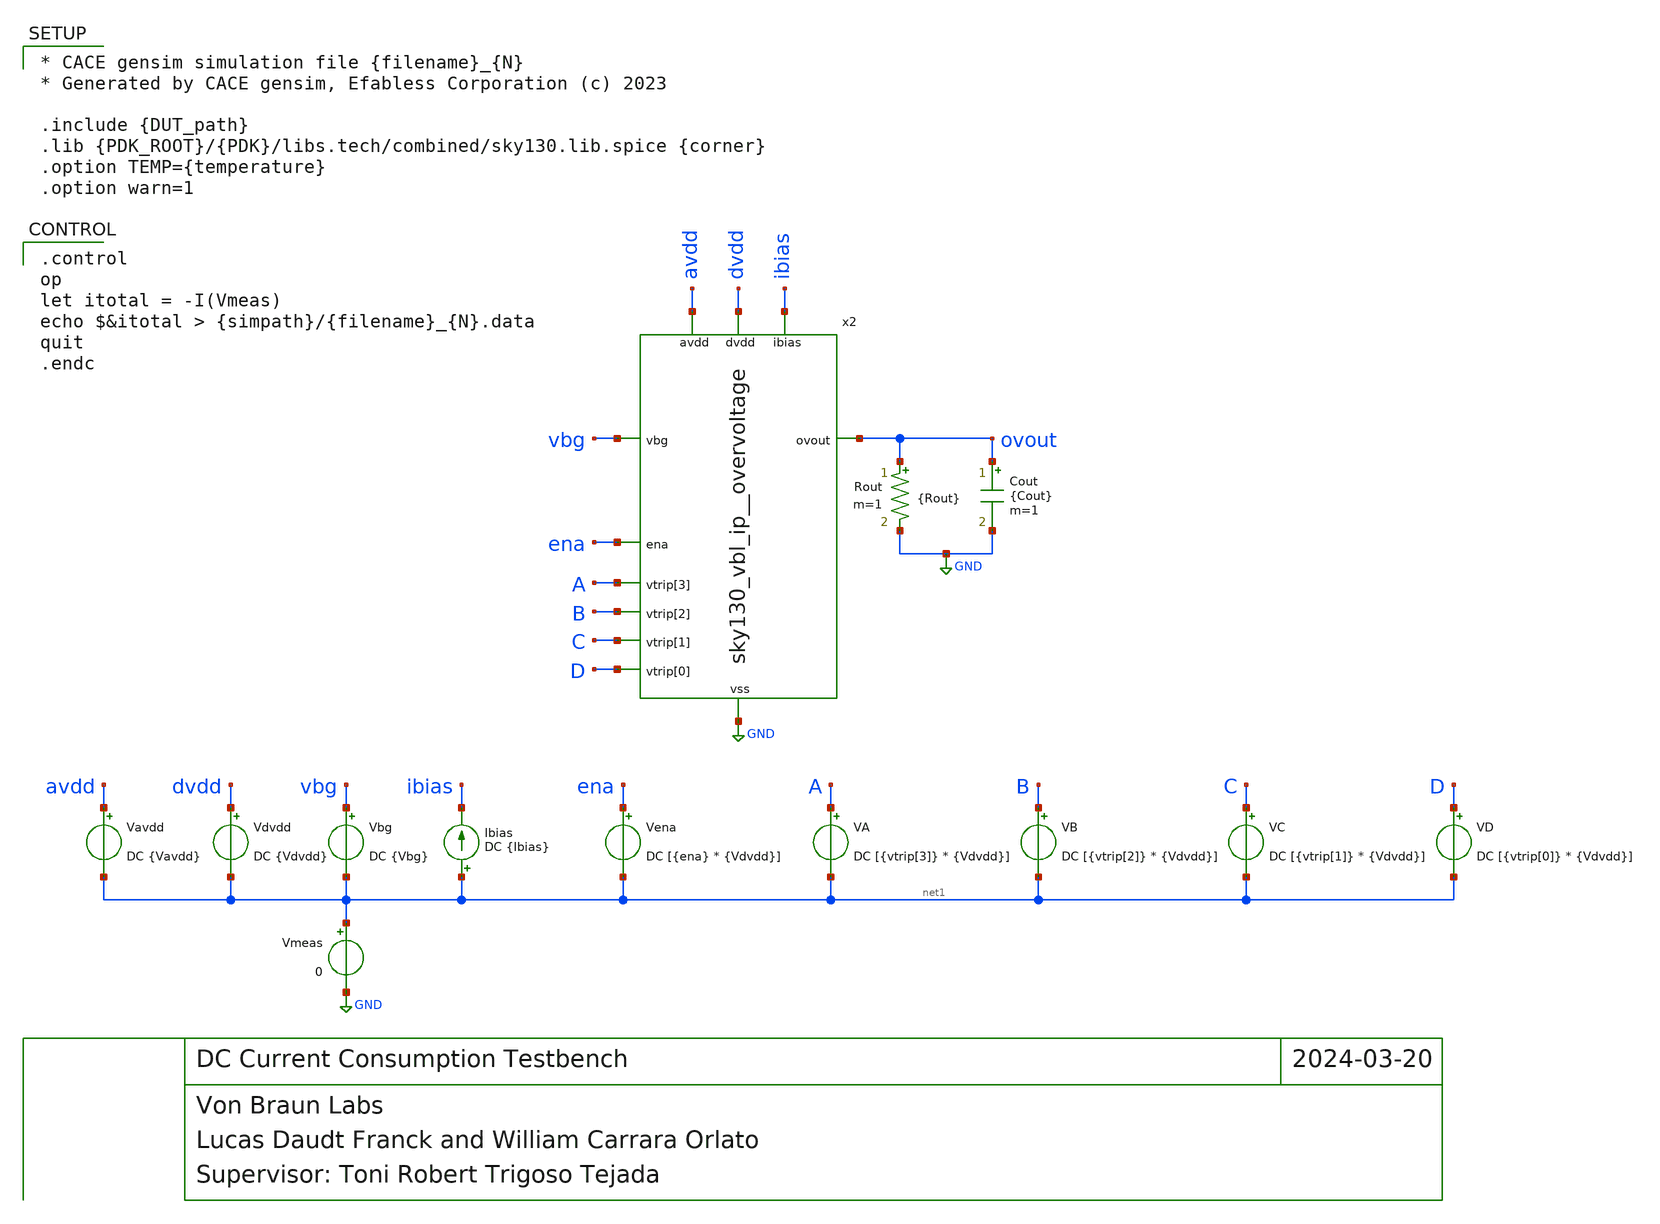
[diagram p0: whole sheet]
** sch_path: cace/tb_dccurrent.sch
**.subckt tb_dccurrent
Cout ovout GND {Cout} m=1
Rout ovout GND {Rout} m=1
Vavdd avdd net1 DC {Vavdd}
Vdvdd dvdd net1 DC {Vdvdd}
Vena ena net1 DC [{ena} * {Vdvdd}]
VA A net1 DC [{vtrip[3]} * {Vdvdd}]
VB B net1 DC [{vtrip[2]} * {Vdvdd}]
VC C net1 DC [{vtrip[1]} * {Vdvdd}]
VD D net1 DC [{vtrip[0]} * {Vdvdd}]
Vbg vbg net1 DC {Vbg}
Ibias net1 ibias DC {Ibias}
Vmeas net1 GND 0
x2 avdd dvdd ena A GND ibias B ovout vbg C D sky130_vbl_ip__overvoltage
**** begin user architecture code

* CACE gensim simulation file {filename}_{N}
* Generated by CACE gensim, Efabless Corporation (c) 2023

.include {DUT_path}
.lib {PDK_ROOT}/{PDK}/libs.tech/combined/sky130.lib.spice {corner}
.option TEMP={temperature}
.option warn=1



.control
op
let itotal = -I(Vmeas)
echo $&itotal > {simpath}/{filename}_{N}.data
quit
.endc


**** end user architecture code
**.ends
.GLOBAL GND
.end
